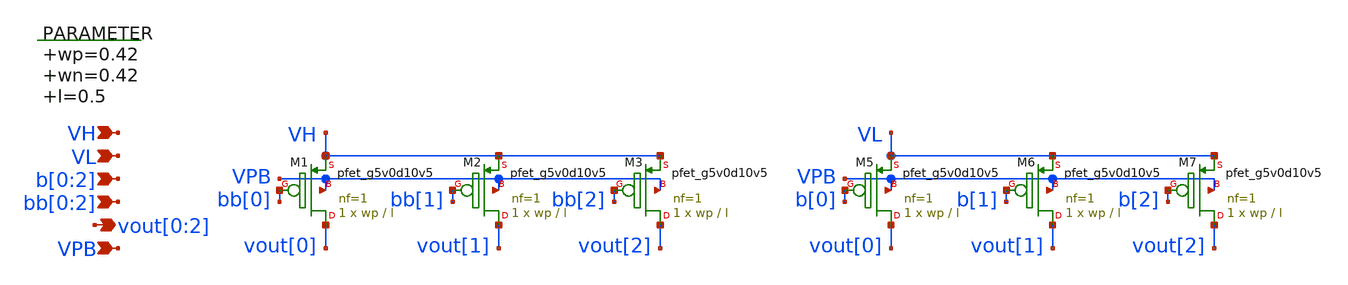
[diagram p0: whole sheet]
** sch_path: xschem/interpolating_dec_3b.sch
**.subckt interpolating_dec_3b vout[0],vout[1],vout[2] b[0],b[1],b[2] VPB VH VL bb[0],bb[1],bb[2]
*.opin vout[0],vout[1],vout[2]
*.ipin b[0],b[1],b[2]
*.ipin VPB
*.ipin VH
*.ipin VL
*.ipin bb[0],bb[1],bb[2]
.param wp=0.42 wn=0.42 l=0.5

XM5 vout[0] b[0] VL VPB sky130_fd_pr__pfet_g5v0d10v5 L=l W=wp nf=1 ad='int((nf+1)/2) * W/nf * 0.29' as='int((nf+2)/2) * W/nf * 0.29'
+ pd='2*int((nf+1)/2) * (W/nf + 0.29)' ps='2*int((nf+2)/2) * (W/nf + 0.29)' nrd='0.29 / W' nrs='0.29 / W'
+ sa=0 sb=0 sd=0 mult=1 m=1
XM6 vout[1] b[1] VL VPB sky130_fd_pr__pfet_g5v0d10v5 L=l W=wp nf=1 ad='int((nf+1)/2) * W/nf * 0.29' as='int((nf+2)/2) * W/nf * 0.29'
+ pd='2*int((nf+1)/2) * (W/nf + 0.29)' ps='2*int((nf+2)/2) * (W/nf + 0.29)' nrd='0.29 / W' nrs='0.29 / W'
+ sa=0 sb=0 sd=0 mult=1 m=1
XM7 vout[2] b[2] VL VPB sky130_fd_pr__pfet_g5v0d10v5 L=l W=wp nf=1 ad='int((nf+1)/2) * W/nf * 0.29' as='int((nf+2)/2) * W/nf * 0.29'
+ pd='2*int((nf+1)/2) * (W/nf + 0.29)' ps='2*int((nf+2)/2) * (W/nf + 0.29)' nrd='0.29 / W' nrs='0.29 / W'
+ sa=0 sb=0 sd=0 mult=1 m=1
XM1 vout[0] bb[0] VH VPB sky130_fd_pr__pfet_g5v0d10v5 L=l W=wp nf=1 ad='int((nf+1)/2) * W/nf * 0.29'
+ as='int((nf+2)/2) * W/nf * 0.29' pd='2*int((nf+1)/2) * (W/nf + 0.29)' ps='2*int((nf+2)/2) * (W/nf + 0.29)'
+ nrd='0.29 / W' nrs='0.29 / W' sa=0 sb=0 sd=0 mult=1 m=1
XM2 vout[1] bb[1] VH VPB sky130_fd_pr__pfet_g5v0d10v5 L=l W=wp nf=1 ad='int((nf+1)/2) * W/nf * 0.29'
+ as='int((nf+2)/2) * W/nf * 0.29' pd='2*int((nf+1)/2) * (W/nf + 0.29)' ps='2*int((nf+2)/2) * (W/nf + 0.29)'
+ nrd='0.29 / W' nrs='0.29 / W' sa=0 sb=0 sd=0 mult=1 m=1
XM3 vout[2] bb[2] VH VPB sky130_fd_pr__pfet_g5v0d10v5 L=l W=wp nf=1 ad='int((nf+1)/2) * W/nf * 0.29'
+ as='int((nf+2)/2) * W/nf * 0.29' pd='2*int((nf+1)/2) * (W/nf + 0.29)' ps='2*int((nf+2)/2) * (W/nf + 0.29)'
+ nrd='0.29 / W' nrs='0.29 / W' sa=0 sb=0 sd=0 mult=1 m=1
**.ends
.end
